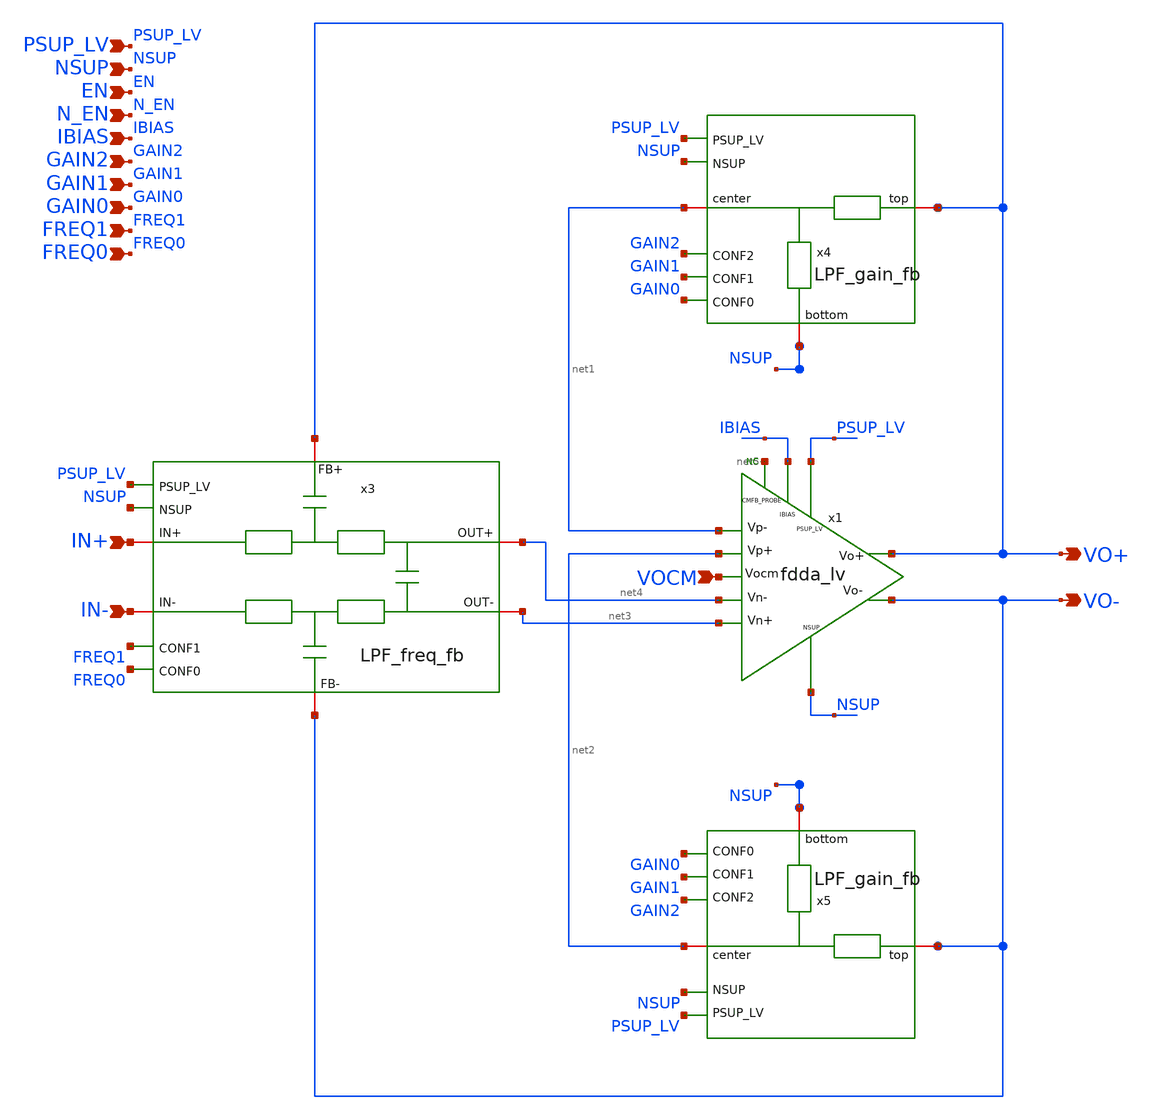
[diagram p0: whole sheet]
** sch_path: xschem/blocks/LPF/LPF.sch
**.subckt LPF NSUP EN N_EN IBIAS PSUP_LV GAIN2 VO+ VO- GAIN1 GAIN0 FREQ1 FREQ0 IN+ IN- VOCM
*.ipin NSUP
*.ipin EN
*.ipin N_EN
*.ipin IBIAS
*.ipin PSUP_LV
*.ipin GAIN2
*.opin VO+
*.opin VO-
*.ipin GAIN1
*.ipin GAIN0
*.ipin FREQ1
*.ipin FREQ0
*.ipin IN+
*.ipin IN-
*.ipin VOCM
* noconn #net5
x1 PSUP_LV net1 net4 net3 net2 VO+ VO- IBIAS NSUP net5 VOCM fdda_lv
x3 VO+ PSUP_LV NSUP net4 IN+ FREQ1 FREQ0 net3 IN- VO- LPF_freq_fb
x4 VO+ net1 PSUP_LV NSUP GAIN2 GAIN1 GAIN0 NSUP LPF_gain_fb
x5 VO- net2 PSUP_LV NSUP GAIN2 GAIN1 GAIN0 NSUP LPF_gain_fb
**.ends
.end
